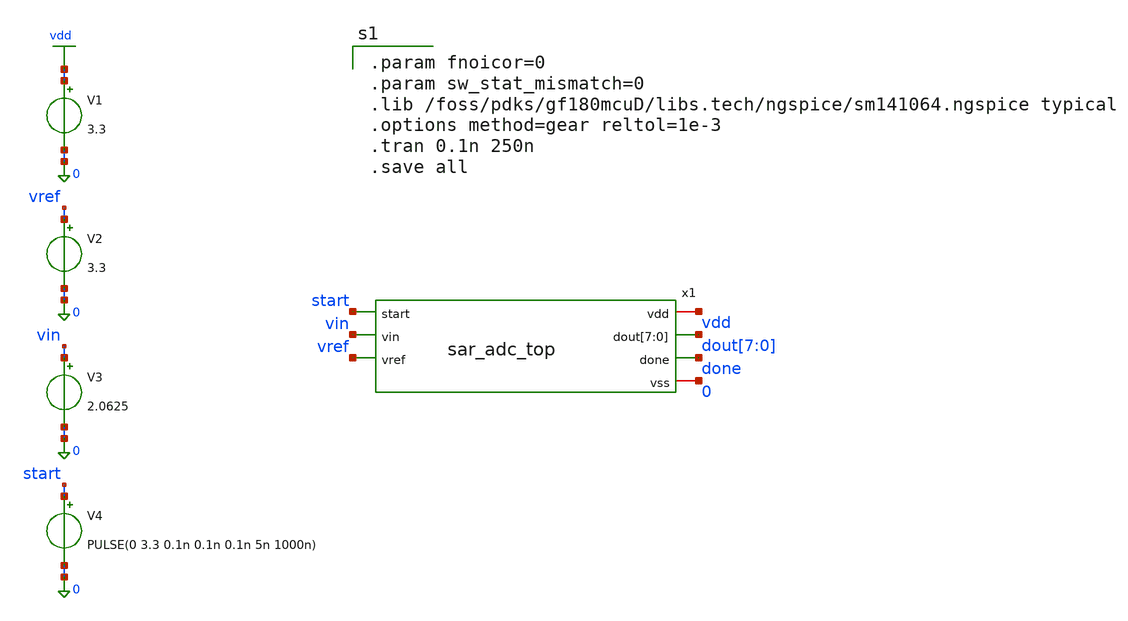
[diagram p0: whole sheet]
** sch_path: xschem/sar_adc/tb_sar_adc_top.sch
**.subckt tb_sar_adc_top
V1 vdd 0 3.3
V2 vref 0 3.3
V3 vin 0 2.0625
V4 start 0 PULSE(0 3.3 0.1n 0.1n 0.1n 5n 1000n)
x1 vdd start vin dout[7] dout[6] dout[5] dout[4] dout[3] dout[2] dout[1] dout[0] done vref 0
+ sar_adc_top
**** begin user architecture code

.param fnoicor=0
.param sw_stat_mismatch=0
.lib /foss/pdks/gf180mcuD/libs.tech/ngspice/sm141064.ngspice typical
.options method=gear reltol=1e-3
.tran 0.1n 250n
.save all

**** end user architecture code
**.ends
.GLOBAL vdd
.end
